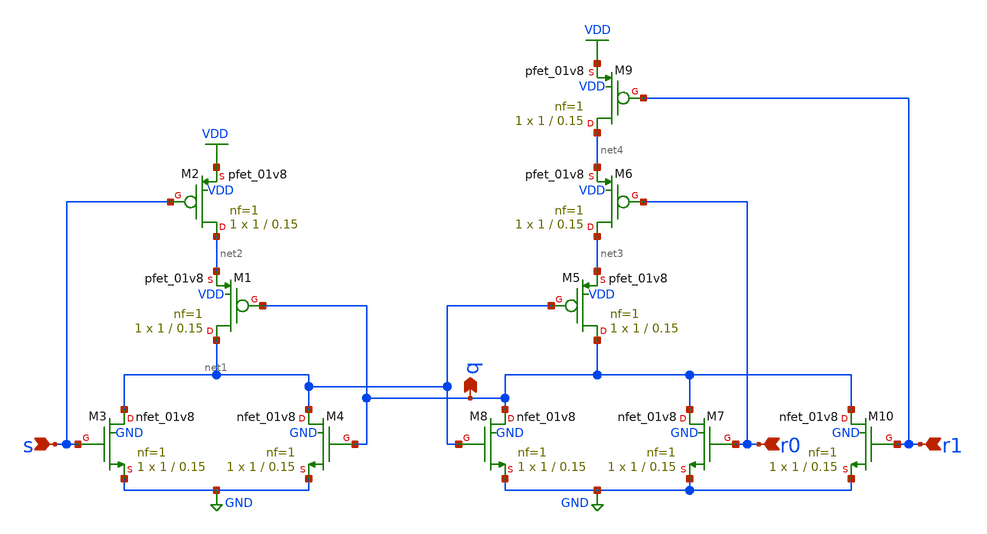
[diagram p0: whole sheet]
** sch_path: xschem/sr_latch.sch
**.subckt sr_latch s r0 q r1
*.ipin s
*.ipin r0
*.opin q
*.ipin r1
XM1 net1 q net2 VDD sky130_fd_pr__pfet_01v8 L=0.15 W=1 nf=1 ad='int((1 + 1)/2) * 1 / 1 * 0.29' as='int((1 + 2)/2) * 1 / 1 * 0.29'
+ pd='2*int((1 + 1)/2) * (1 / 1 + 0.29)' ps='2*int((1 + 2)/2) * (1 / 1 + 0.29)' nrd='0.29 / 1 ' nrs='0.29 / 1 '
+ sa=0 sb=0 sd=0 mult=1 m=1
XM2 net2 s VDD VDD sky130_fd_pr__pfet_01v8 L=0.15 W=1 nf=1 ad='int((1 + 1)/2) * 1 / 1 * 0.29' as='int((1 + 2)/2) * 1 / 1 * 0.29'
+ pd='2*int((1 + 1)/2) * (1 / 1 + 0.29)' ps='2*int((1 + 2)/2) * (1 / 1 + 0.29)' nrd='0.29 / 1 ' nrs='0.29 / 1 '
+ sa=0 sb=0 sd=0 mult=1 m=1
XM3 net1 s GND GND sky130_fd_pr__nfet_01v8 L=0.15 W=1 nf=1 ad='int((1 + 1)/2) * 1 / 1 * 0.29' as='int((1 + 2)/2) * 1 / 1 * 0.29'
+ pd='2*int((1 + 1)/2) * (1 / 1 + 0.29)' ps='2*int((1 + 2)/2) * (1 / 1 + 0.29)' nrd='0.29 / 1 ' nrs='0.29 / 1 '
+ sa=0 sb=0 sd=0 mult=1 m=1
XM4 net1 q GND GND sky130_fd_pr__nfet_01v8 L=0.15 W=1 nf=1 ad='int((1 + 1)/2) * 1 / 1 * 0.29' as='int((1 + 2)/2) * 1 / 1 * 0.29'
+ pd='2*int((1 + 1)/2) * (1 / 1 + 0.29)' ps='2*int((1 + 2)/2) * (1 / 1 + 0.29)' nrd='0.29 / 1 ' nrs='0.29 / 1 '
+ sa=0 sb=0 sd=0 mult=1 m=1
XM5 q net1 net3 VDD sky130_fd_pr__pfet_01v8 L=0.15 W=1 nf=1 ad='int((1 + 1)/2) * 1 / 1 * 0.29' as='int((1 + 2)/2) * 1 / 1 * 0.29'
+ pd='2*int((1 + 1)/2) * (1 / 1 + 0.29)' ps='2*int((1 + 2)/2) * (1 / 1 + 0.29)' nrd='0.29 / 1 ' nrs='0.29 / 1 '
+ sa=0 sb=0 sd=0 mult=1 m=1
XM6 net3 r0 net4 VDD sky130_fd_pr__pfet_01v8 L=0.15 W=1 nf=1 ad='int((1 + 1)/2) * 1 / 1 * 0.29' as='int((1 + 2)/2) * 1 / 1 * 0.29'
+ pd='2*int((1 + 1)/2) * (1 / 1 + 0.29)' ps='2*int((1 + 2)/2) * (1 / 1 + 0.29)' nrd='0.29 / 1 ' nrs='0.29 / 1 '
+ sa=0 sb=0 sd=0 mult=1 m=1
XM7 q r0 GND GND sky130_fd_pr__nfet_01v8 L=0.15 W=1 nf=1 ad='int((1 + 1)/2) * 1 / 1 * 0.29' as='int((1 + 2)/2) * 1 / 1 * 0.29'
+ pd='2*int((1 + 1)/2) * (1 / 1 + 0.29)' ps='2*int((1 + 2)/2) * (1 / 1 + 0.29)' nrd='0.29 / 1 ' nrs='0.29 / 1 '
+ sa=0 sb=0 sd=0 mult=1 m=1
XM8 q net1 GND GND sky130_fd_pr__nfet_01v8 L=0.15 W=1 nf=1 ad='int((1 + 1)/2) * 1 / 1 * 0.29' as='int((1 + 2)/2) * 1 / 1 * 0.29'
+ pd='2*int((1 + 1)/2) * (1 / 1 + 0.29)' ps='2*int((1 + 2)/2) * (1 / 1 + 0.29)' nrd='0.29 / 1 ' nrs='0.29 / 1 '
+ sa=0 sb=0 sd=0 mult=1 m=1
XM9 net4 r1 VDD VDD sky130_fd_pr__pfet_01v8 L=0.15 W=1 nf=1 ad='int((1 + 1)/2) * 1 / 1 * 0.29' as='int((1 + 2)/2) * 1 / 1 * 0.29'
+ pd='2*int((1 + 1)/2) * (1 / 1 + 0.29)' ps='2*int((1 + 2)/2) * (1 / 1 + 0.29)' nrd='0.29 / 1 ' nrs='0.29 / 1 '
+ sa=0 sb=0 sd=0 mult=1 m=1
XM10 q r1 GND GND sky130_fd_pr__nfet_01v8 L=0.15 W=1 nf=1 ad='int((1 + 1)/2) * 1 / 1 * 0.29' as='int((1 + 2)/2) * 1 / 1 * 0.29'
+ pd='2*int((1 + 1)/2) * (1 / 1 + 0.29)' ps='2*int((1 + 2)/2) * (1 / 1 + 0.29)' nrd='0.29 / 1 ' nrs='0.29 / 1 '
+ sa=0 sb=0 sd=0 mult=1 m=1
**.ends
.GLOBAL VDD
.GLOBAL GND
.end
